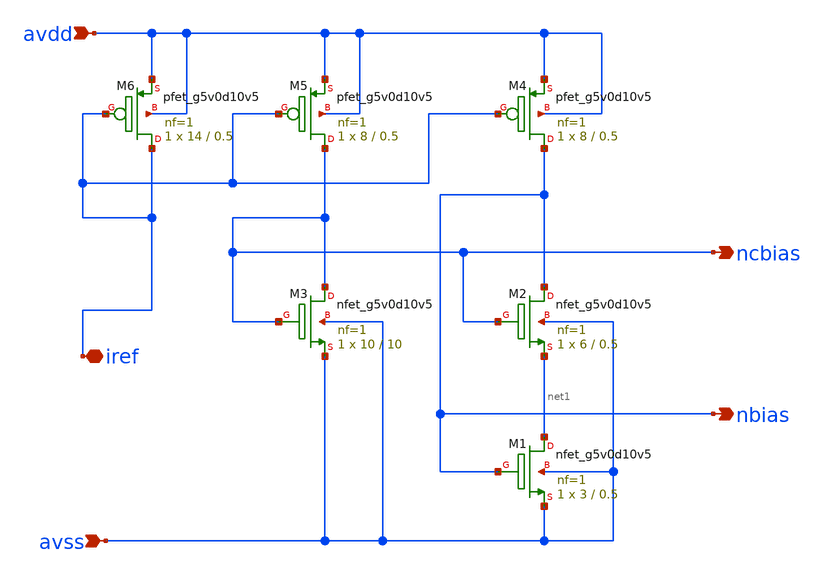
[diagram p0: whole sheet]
** sch_path: xschem/n_ibias.sch
**.subckt n_ibias avss avdd iref nbias ncbias
*.ipin avss
*.ipin avdd
*.iopin iref
*.opin nbias
*.opin ncbias
XM1 net1 nbias avss avss sky130_fd_pr__nfet_g5v0d10v5 L=0.5 W=3 nf=1 ad='int((nf+1)/2) * W/nf * 0.29'
+ as='int((nf+2)/2) * W/nf * 0.29' pd='2*int((nf+1)/2) * (W/nf + 0.29)' ps='2*int((nf+2)/2) * (W/nf + 0.29)'
+ nrd='0.29 / W' nrs='0.29 / W' sa=0 sb=0 sd=0 mult=1 m=1
XM2 nbias ncbias net1 avss sky130_fd_pr__nfet_g5v0d10v5 L=0.5 W=6 nf=1 ad='int((nf+1)/2) * W/nf * 0.29'
+ as='int((nf+2)/2) * W/nf * 0.29' pd='2*int((nf+1)/2) * (W/nf + 0.29)' ps='2*int((nf+2)/2) * (W/nf + 0.29)'
+ nrd='0.29 / W' nrs='0.29 / W' sa=0 sb=0 sd=0 mult=1 m=1
XM3 ncbias ncbias avss avss sky130_fd_pr__nfet_g5v0d10v5 L=10 W=10 nf=1 ad='int((nf+1)/2) * W/nf * 0.29'
+ as='int((nf+2)/2) * W/nf * 0.29' pd='2*int((nf+1)/2) * (W/nf + 0.29)' ps='2*int((nf+2)/2) * (W/nf + 0.29)'
+ nrd='0.29 / W' nrs='0.29 / W' sa=0 sb=0 sd=0 mult=1 m=1
XM4 nbias iref avdd avdd sky130_fd_pr__pfet_g5v0d10v5 L=0.5 W=8 nf=1 ad='int((nf+1)/2) * W/nf * 0.29'
+ as='int((nf+2)/2) * W/nf * 0.29' pd='2*int((nf+1)/2) * (W/nf + 0.29)' ps='2*int((nf+2)/2) * (W/nf + 0.29)'
+ nrd='0.29 / W' nrs='0.29 / W' sa=0 sb=0 sd=0 mult=1 m=1
XM5 ncbias iref avdd avdd sky130_fd_pr__pfet_g5v0d10v5 L=0.5 W=8 nf=1 ad='int((nf+1)/2) * W/nf * 0.29'
+ as='int((nf+2)/2) * W/nf * 0.29' pd='2*int((nf+1)/2) * (W/nf + 0.29)' ps='2*int((nf+2)/2) * (W/nf + 0.29)'
+ nrd='0.29 / W' nrs='0.29 / W' sa=0 sb=0 sd=0 mult=1 m=1
XM6 iref iref avdd avdd sky130_fd_pr__pfet_g5v0d10v5 L=0.5 W=14 nf=1 ad='int((nf+1)/2) * W/nf * 0.29'
+ as='int((nf+2)/2) * W/nf * 0.29' pd='2*int((nf+1)/2) * (W/nf + 0.29)' ps='2*int((nf+2)/2) * (W/nf + 0.29)'
+ nrd='0.29 / W' nrs='0.29 / W' sa=0 sb=0 sd=0 mult=1 m=1
**.ends
.end
